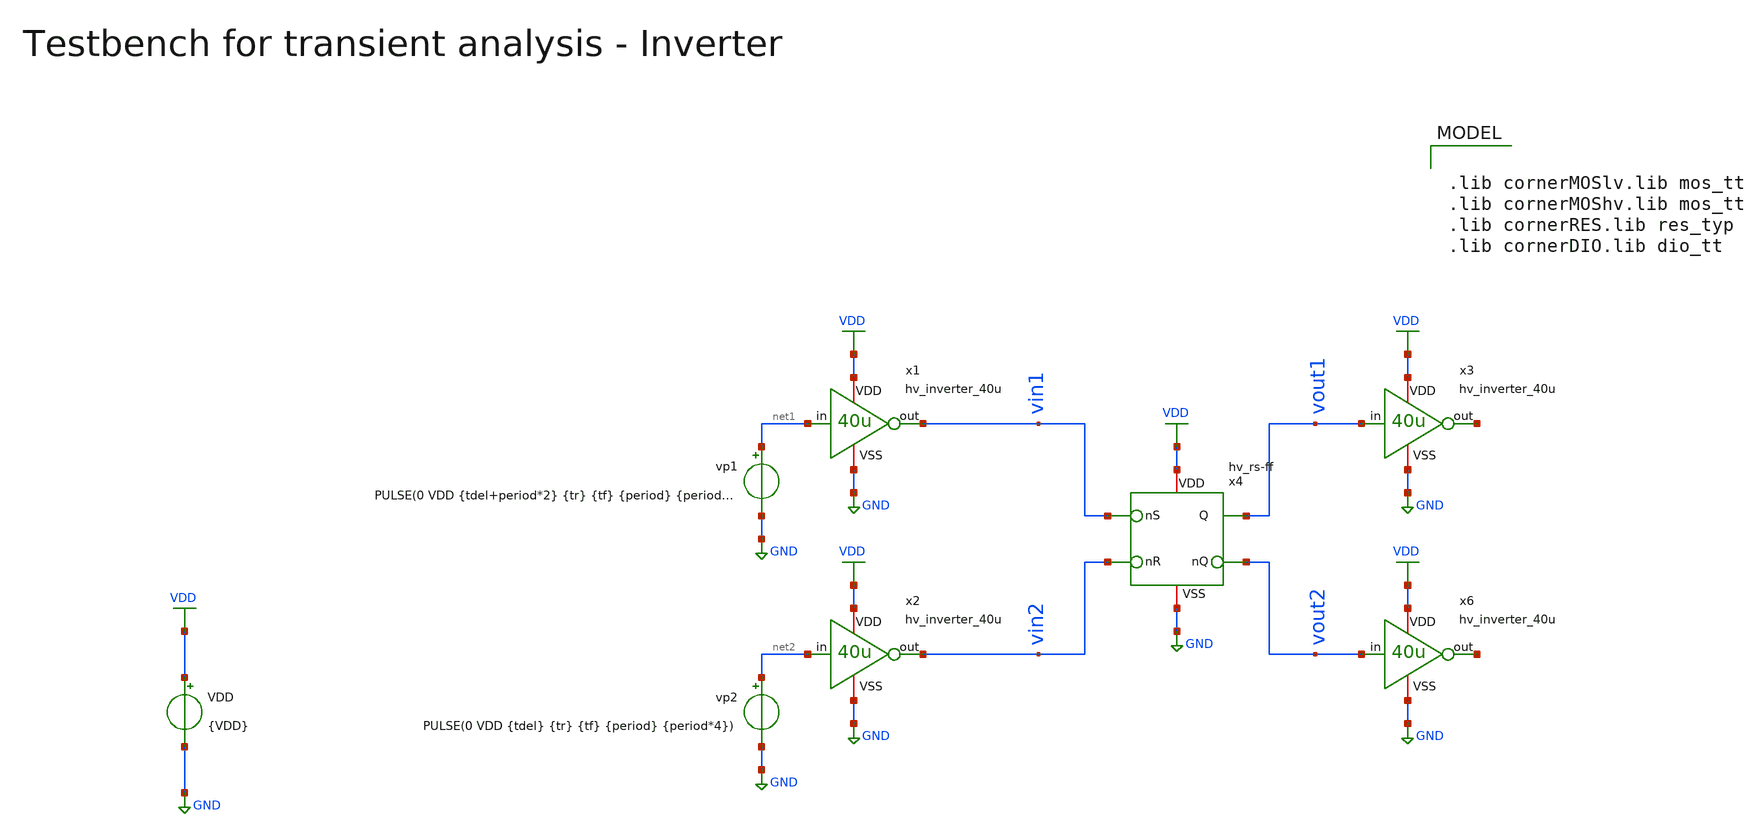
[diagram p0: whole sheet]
** sch_path: macros/heichips26_vcr/macros/switched_capacitor/testbenches/xschem/tb_hv_rs-ff_tran.sch
**.subckt tb_hv_rs-ff_tran
VDD VDD GND {VDD}
vp2 net2 GND PULSE(0 VDD {tdel} {tr} {tf} {period} {period*4})
vp1 net1 GND PULSE(0 VDD {tdel+period*2} {tr} {tf} {period} {period*4})
x1 VDD net1 vin1 GND hv_inverter_40u
x2 VDD net2 vin2 GND hv_inverter_40u
x3 VDD vout1 net3 GND hv_inverter_40u
x6 VDD vout2 net4 GND hv_inverter_40u
x4 VDD vin1 vout1 vout2 vin2 GND hv_rs-ff
**** begin user architecture code


.ic v(vout2)=0

.param VDD=3.3
.csparam VDD=VDD
.param Vcm=VDD/2
.param temp=27
.param Cload=10p
.param Rload=1k

.param period = 1n
.param tdel   = {period/2}
.param ton    = {period*2}
.csparam tstop  = {5*period}
.csparam tstep  = {period/100}
.param tr     = {period/100}
.param tf     = {period/100}

.options savecurrents klu method=gear reltol=1e-4 abstol=1e-15 gmin=1e-15
.control

save all

* Operating Point Analysis
op
remzerovec
write @schname\.raw
set appendwrite

* Transient Analysis
tran {$&tstep} {$&tstop}
write @schname\.raw

* Plotting
plot vin1+12 vin2+8 vout1+4 vout2

* Write Data
unset appendwrite
set wr_vecnames
set wr_singlescale
wrdata ../plot_simulations/data/@schname\.txt v(vin1) v(vin2) v(vout)

*quit
.endc



.lib cornerMOSlv.lib mos_tt
.lib cornerMOShv.lib mos_tt
.lib cornerRES.lib res_typ
.lib cornerDIO.lib dio_tt

**** end user architecture code
**.ends

* expanding   symbol:  hv_inverter_40u.sym # of pins=4
** sym_path: macros/heichips26_vcr/macros/switched_capacitor/schematic/xschem/hv_inverter_40u.sym
** sch_path: macros/heichips26_vcr/macros/switched_capacitor/schematic/xschem/hv_inverter_40u.sch
.subckt hv_inverter_40u VDD in out VSS
*.ipin in
*.iopin VDD
*.iopin VSS
*.opin out
XM2 out in VSS VSS sg13_hv_nmos w={n_w} l={n_l} ng={ng} m=1 mm_ok=1
XM3 out in VDD VDD sg13_hv_pmos w={p_w} l={p_l} ng={ng} m=1 mm_ok=1
**** begin user architecture code


.param w   = 10u
.param ng  = 4
.param n_ng = ng
.param n_w = {3u*n_ng}
.param n_l = 0.45u
.param p_ng = ng
.param p_w = {10u*p_ng}
.param p_l = 0.4u


**** end user architecture code
.ends


* expanding   symbol:  hv_rs-ff.sym # of pins=6
** sym_path: macros/heichips26_vcr/macros/switched_capacitor/schematic/xschem/hv_rs-ff.sym
** sch_path: macros/heichips26_vcr/macros/switched_capacitor/schematic/xschem/hv_rs-ff.sch
.subckt hv_rs-ff VDD nS Q nQ nR VSS
*.ipin nS
*.iopin VDD
*.iopin VSS
*.opin Q
*.ipin nR
*.opin nQ
x4 VDD nS Q nQ VSS hv_nand
x5 VDD Q nQ nR VSS hv_nand
.ends


* expanding   symbol:  hv_nand.sym # of pins=5
** sym_path: macros/heichips26_vcr/macros/switched_capacitor/schematic/xschem/hv_nand.sym
** sch_path: macros/heichips26_vcr/macros/switched_capacitor/schematic/xschem/hv_nand.sch
.subckt hv_nand VDD in1 out in2 VSS
*.ipin in1
*.iopin VDD
*.iopin VSS
*.opin out
*.ipin in2
**** begin user architecture code


.param w   = 10u
.param ng  = 4
.param n_ng = ng
.param n_w = {3u*n_ng}
.param n_l = 0.45u
.param p_ng = ng
.param p_w = {10u*p_ng}
.param p_l = 0.4u


**** end user architecture code
XM2 out in1 net1 VSS sg13_hv_nmos w={n_w} l={n_l} ng={ng} m=1 mm_ok=1
XM3 out in2 VDD VDD sg13_hv_pmos w={p_w} l={p_l} ng={ng} m=1 mm_ok=1
XM1 net1 in2 VSS VSS sg13_hv_nmos w={n_w} l={n_l} ng={ng} m=1 mm_ok=1
XM4 out in1 VDD VDD sg13_hv_pmos w={p_w} l={p_l} ng={ng} m=1 mm_ok=1
.ends

.GLOBAL GND
.GLOBAL VDD
.end
